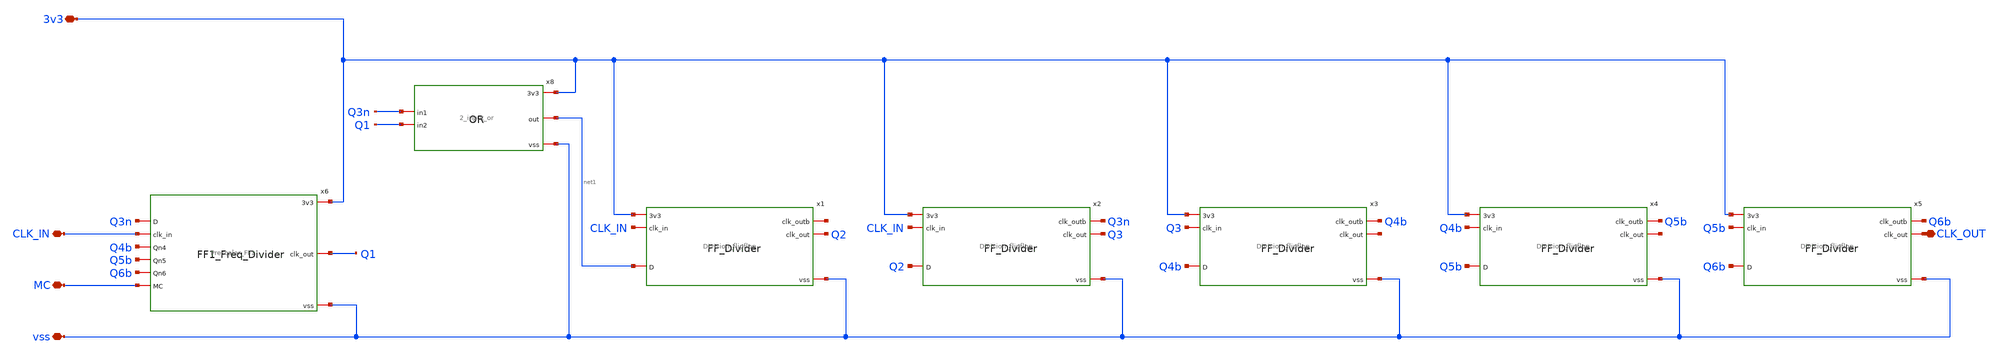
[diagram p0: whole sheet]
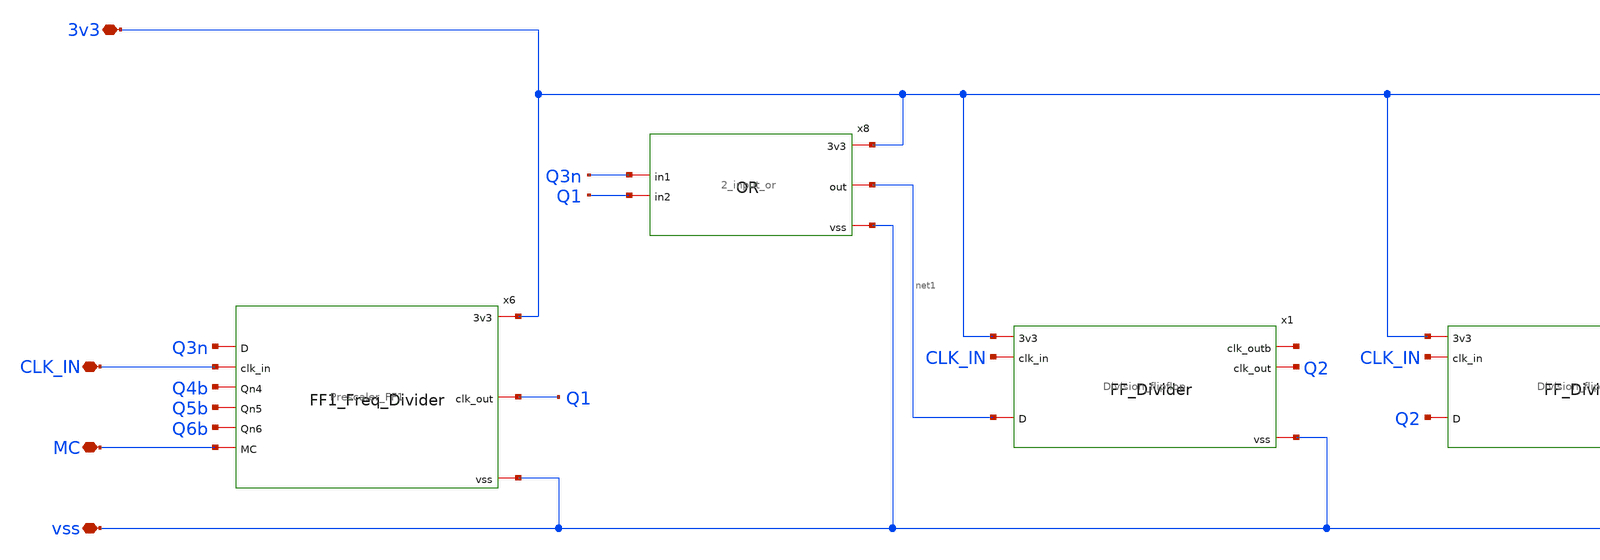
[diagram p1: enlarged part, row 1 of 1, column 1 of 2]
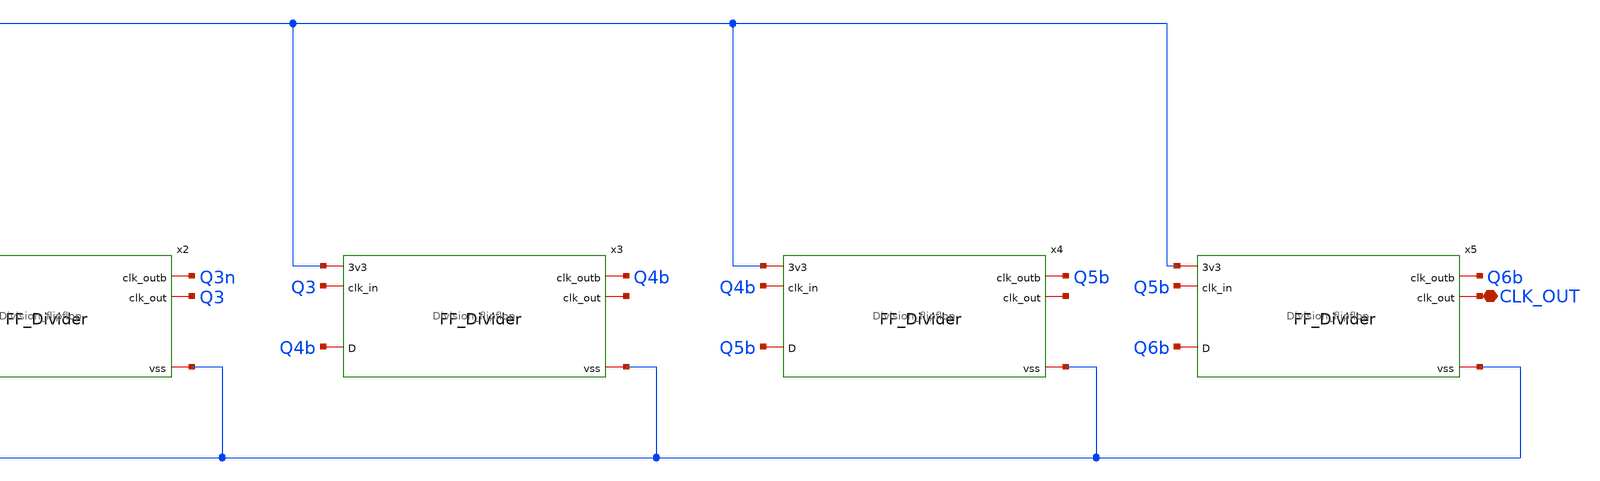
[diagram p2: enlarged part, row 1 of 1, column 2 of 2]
** sch_path: PLL/analog/schematics/32_33_Prescaler_Block.sch
**.subckt 32_33_Prescaler_Block CLK_IN MC 3v3 vss CLK_OUT
*.iopin CLK_IN
*.iopin MC
*.iopin 3v3
*.iopin vss
*.iopin CLK_OUT
x8 3v3 Q3n Q1 net1 vss 2_input_or
x6 3v3 Q1 Q3n CLK_IN Q4b Q5b Q6b MC vss Prescaler_FF1
x1 3v3 CLK_IN net2 Q2 net1 vss Division_flipflop
x2 3v3 CLK_IN Q3n Q3 Q2 vss Division_flipflop
x3 3v3 Q3 Q4b net3 Q4b vss Division_flipflop
x4 3v3 Q4b Q5b net4 Q5b vss Division_flipflop
x5 3v3 Q5b Q6b CLK_OUT Q6b vss Division_flipflop
**.ends

* expanding   symbol:  2_input_or.sym # of pins=5
** sym_path: PLL/analog/schematics/2_input_or.sym
** sch_path: PLL/analog/schematics/2_input_or.sch
.subckt 2_input_or 3v3 in1 in2 out vss
*.iopin in1
*.iopin in2
*.iopin out
*.iopin 3v3
*.iopin vss
XM1 net1 in1 3v3 3v3 pfet_03v3 L=0.36u W=0.72u nf=1 ad='int((nf+1)/2) * W/nf * 0.18u' as='int((nf+2)/2) * W/nf * 0.18u'
+ pd='2*int((nf+1)/2) * (W/nf + 0.18u)' ps='2*int((nf+2)/2) * (W/nf + 0.18u)' nrd='0.18u / W' nrs='0.18u / W'
+ sa=0 sb=0 sd=0 m=1
XM2 net2 in2 net1 3v3 pfet_03v3 L=0.36u W=0.72u nf=1 ad='int((nf+1)/2) * W/nf * 0.18u' as='int((nf+2)/2) * W/nf * 0.18u'
+ pd='2*int((nf+1)/2) * (W/nf + 0.18u)' ps='2*int((nf+2)/2) * (W/nf + 0.18u)' nrd='0.18u / W' nrs='0.18u / W'
+ sa=0 sb=0 sd=0 m=1
XM3 net2 in1 vss vss nfet_03v3 L=0.36u W=0.36u nf=1 ad='int((nf+1)/2) * W/nf * 0.18u' as='int((nf+2)/2) * W/nf * 0.18u'
+ pd='2*int((nf+1)/2) * (W/nf + 0.18u)' ps='2*int((nf+2)/2) * (W/nf + 0.18u)' nrd='0.18u / W' nrs='0.18u / W'
+ sa=0 sb=0 sd=0 m=1
XM4 net2 in2 vss vss nfet_03v3 L=0.36u W=0.36u nf=1 ad='int((nf+1)/2) * W/nf * 0.18u' as='int((nf+2)/2) * W/nf * 0.18u'
+ pd='2*int((nf+1)/2) * (W/nf + 0.18u)' ps='2*int((nf+2)/2) * (W/nf + 0.18u)' nrd='0.18u / W' nrs='0.18u / W'
+ sa=0 sb=0 sd=0 m=1
XM5 out net2 vss vss nfet_03v3 L=0.36u W=0.36u nf=1 ad='int((nf+1)/2) * W/nf * 0.18u' as='int((nf+2)/2) * W/nf * 0.18u'
+ pd='2*int((nf+1)/2) * (W/nf + 0.18u)' ps='2*int((nf+2)/2) * (W/nf + 0.18u)' nrd='0.18u / W' nrs='0.18u / W'
+ sa=0 sb=0 sd=0 m=1
XM6 out net2 3v3 3v3 pfet_03v3 L=0.36u W=0.72u nf=1 ad='int((nf+1)/2) * W/nf * 0.18u' as='int((nf+2)/2) * W/nf * 0.18u'
+ pd='2*int((nf+1)/2) * (W/nf + 0.18u)' ps='2*int((nf+2)/2) * (W/nf + 0.18u)' nrd='0.18u / W' nrs='0.18u / W'
+ sa=0 sb=0 sd=0 m=1
.ends


* expanding   symbol:  Prescaler_FF1.sym # of pins=9
** sym_path: PLL/analog/schematics/Prescaler_FF1.sym
** sch_path: PLL/analog/schematics/Prescaler_FF1.sch
.subckt Prescaler_FF1 3v3 clk_out D clk_in Qn4 Qn5 Qn6 MC vss
*.iopin D
*.iopin clk_in
*.iopin Qn4
*.iopin Qn5
*.iopin Qn6
*.iopin vss
*.iopin 3v3
*.iopin MC
*.iopin clk_out
XM1 net8 clk_in 3v3 3v3 pfet_03v3 L=0.32u W=0.72u nf=1 ad='int((nf+1)/2) * W/nf * 0.18u' as='int((nf+2)/2) * W/nf * 0.18u'
+ pd='2*int((nf+1)/2) * (W/nf + 0.18u)' ps='2*int((nf+2)/2) * (W/nf + 0.18u)' nrd='0.18u / W' nrs='0.18u / W'
+ sa=0 sb=0 sd=0 m=1
XM2 net1 D net8 3v3 pfet_03v3 L=0.32u W=0.72u nf=1 ad='int((nf+1)/2) * W/nf * 0.18u' as='int((nf+2)/2) * W/nf * 0.18u'
+ pd='2*int((nf+1)/2) * (W/nf + 0.18u)' ps='2*int((nf+2)/2) * (W/nf + 0.18u)' nrd='0.18u / W' nrs='0.18u / W'
+ sa=0 sb=0 sd=0 m=1
XM3 net1 D net2 vss nfet_03v3 L=0.32u W=0.36u nf=1 ad='int((nf+1)/2) * W/nf * 0.18u' as='int((nf+2)/2) * W/nf * 0.18u'
+ pd='2*int((nf+1)/2) * (W/nf + 0.18u)' ps='2*int((nf+2)/2) * (W/nf + 0.18u)' nrd='0.18u / W' nrs='0.18u / W'
+ sa=0 sb=0 sd=0 m=1
XM4 net2 clk_in net3 vss nfet_03v3 L=0.32u W=0.36u nf=1 ad='int((nf+1)/2) * W/nf * 0.18u' as='int((nf+2)/2) * W/nf * 0.18u'
+ pd='2*int((nf+1)/2) * (W/nf + 0.18u)' ps='2*int((nf+2)/2) * (W/nf + 0.18u)' nrd='0.18u / W' nrs='0.18u / W'
+ sa=0 sb=0 sd=0 m=1
XM5 net3 Qn4 net4 vss nfet_03v3 L=0.32u W=0.36u nf=1 ad='int((nf+1)/2) * W/nf * 0.18u' as='int((nf+2)/2) * W/nf * 0.18u'
+ pd='2*int((nf+1)/2) * (W/nf + 0.18u)' ps='2*int((nf+2)/2) * (W/nf + 0.18u)' nrd='0.18u / W' nrs='0.18u / W'
+ sa=0 sb=0 sd=0 m=1
XM6 net4 Qn5 net5 vss nfet_03v3 L=0.32u W=0.36u nf=1 ad='int((nf+1)/2) * W/nf * 0.18u' as='int((nf+2)/2) * W/nf * 0.18u'
+ pd='2*int((nf+1)/2) * (W/nf + 0.18u)' ps='2*int((nf+2)/2) * (W/nf + 0.18u)' nrd='0.18u / W' nrs='0.18u / W'
+ sa=0 sb=0 sd=0 m=1
XM7 net5 Qn6 net6 vss nfet_03v3 L=0.32u W=0.36u nf=1 ad='int((nf+1)/2) * W/nf * 0.18u' as='int((nf+2)/2) * W/nf * 0.18u'
+ pd='2*int((nf+1)/2) * (W/nf + 0.18u)' ps='2*int((nf+2)/2) * (W/nf + 0.18u)' nrd='0.18u / W' nrs='0.18u / W'
+ sa=0 sb=0 sd=0 m=1
XM8 net6 MC vss vss nfet_03v3 L=0.32u W=0.36u nf=1 ad='int((nf+1)/2) * W/nf * 0.18u' as='int((nf+2)/2) * W/nf * 0.18u'
+ pd='2*int((nf+1)/2) * (W/nf + 0.18u)' ps='2*int((nf+2)/2) * (W/nf + 0.18u)' nrd='0.18u / W' nrs='0.18u / W'
+ sa=0 sb=0 sd=0 m=1
XM9 clk_out net1 3v3 3v3 pfet_03v3 L=0.36u W=0.72u nf=1 ad='int((nf+1)/2) * W/nf * 0.18u' as='int((nf+2)/2) * W/nf * 0.18u'
+ pd='2*int((nf+1)/2) * (W/nf + 0.18u)' ps='2*int((nf+2)/2) * (W/nf + 0.18u)' nrd='0.18u / W' nrs='0.18u / W'
+ sa=0 sb=0 sd=0 m=1
XM10 clk_out net1 net7 vss nfet_03v3 L=0.36u W=0.36u nf=1 ad='int((nf+1)/2) * W/nf * 0.18u' as='int((nf+2)/2) * W/nf * 0.18u'
+ pd='2*int((nf+1)/2) * (W/nf + 0.18u)' ps='2*int((nf+2)/2) * (W/nf + 0.18u)' nrd='0.18u / W' nrs='0.18u / W'
+ sa=0 sb=0 sd=0 m=1
XM11 net7 clk_in vss vss nfet_03v3 L=0.36u W=0.36u nf=1 ad='int((nf+1)/2) * W/nf * 0.18u' as='int((nf+2)/2) * W/nf * 0.18u'
+ pd='2*int((nf+1)/2) * (W/nf + 0.18u)' ps='2*int((nf+2)/2) * (W/nf + 0.18u)' nrd='0.18u / W' nrs='0.18u / W'
+ sa=0 sb=0 sd=0 m=1
.ends


* expanding   symbol:  Division_flipflop.sym # of pins=6
** sym_path: PLL/analog/schematics/Division_flipflop.sym
** sch_path: PLL/analog/schematics/Division_flipflop.sch
.subckt Division_flipflop 3v3 clk_in clk_outb clk_out D vss
*.iopin 3v3
*.iopin vss
*.iopin clk_outb
*.iopin D
*.iopin clk_in
*.iopin clk_out
XM1 net3 clk_in vss vss nfet_03v3 L=0.36u W=0.56u nf=1 ad='int((nf+1)/2) * W/nf * 0.18u' as='int((nf+2)/2) * W/nf * 0.18u'
+ pd='2*int((nf+1)/2) * (W/nf + 0.18u)' ps='2*int((nf+2)/2) * (W/nf + 0.18u)' nrd='0.18u / W' nrs='0.18u / W'
+ sa=0 sb=0 sd=0 m=1
XM2 net2 D vss vss nfet_03v3 L=0.36u W=0.56u nf=1 ad='int((nf+1)/2) * W/nf * 0.18u' as='int((nf+2)/2) * W/nf * 0.18u'
+ pd='2*int((nf+1)/2) * (W/nf + 0.18u)' ps='2*int((nf+2)/2) * (W/nf + 0.18u)' nrd='0.18u / W' nrs='0.18u / W'
+ sa=0 sb=0 sd=0 m=1
XM3 net5 net4 vss vss nfet_03v3 L=0.36u W=0.56u nf=1 ad='int((nf+1)/2) * W/nf * 0.18u' as='int((nf+2)/2) * W/nf * 0.18u'
+ pd='2*int((nf+1)/2) * (W/nf + 0.18u)' ps='2*int((nf+2)/2) * (W/nf + 0.18u)' nrd='0.18u / W' nrs='0.18u / W'
+ sa=0 sb=0 sd=0 m=1
XM4 clk_outb clk_in net5 vss nfet_03v3 L=0.36u W=0.56u nf=1 ad='int((nf+1)/2) * W/nf * 0.18u' as='int((nf+2)/2) * W/nf * 0.18u'
+ pd='2*int((nf+1)/2) * (W/nf + 0.18u)' ps='2*int((nf+2)/2) * (W/nf + 0.18u)' nrd='0.18u / W' nrs='0.18u / W'
+ sa=0 sb=0 sd=0 m=1
XM5 net1 D 3v3 3v3 pfet_03v3 L=0.36u W=1.12u nf=1 ad='int((nf+1)/2) * W/nf * 0.18u' as='int((nf+2)/2) * W/nf * 0.18u'
+ pd='2*int((nf+1)/2) * (W/nf + 0.18u)' ps='2*int((nf+2)/2) * (W/nf + 0.18u)' nrd='0.18u / W' nrs='0.18u / W'
+ sa=0 sb=0 sd=0 m=1
XM6 net2 clk_in net1 3v3 pfet_03v3 L=0.36u W=1.12u nf=1 ad='int((nf+1)/2) * W/nf * 0.18u' as='int((nf+2)/2) * W/nf * 0.18u'
+ pd='2*int((nf+1)/2) * (W/nf + 0.18u)' ps='2*int((nf+2)/2) * (W/nf + 0.18u)' nrd='0.18u / W' nrs='0.18u / W'
+ sa=0 sb=0 sd=0 m=1
XM8 net4 clk_in 3v3 3v3 pfet_03v3 L=0.36u W=1.12u nf=1 ad='int((nf+1)/2) * W/nf * 0.18u' as='int((nf+2)/2) * W/nf * 0.18u'
+ pd='2*int((nf+1)/2) * (W/nf + 0.18u)' ps='2*int((nf+2)/2) * (W/nf + 0.18u)' nrd='0.18u / W' nrs='0.18u / W'
+ sa=0 sb=0 sd=0 m=1
XM9 clk_outb net4 3v3 3v3 pfet_03v3 L=0.36u W=1.12u nf=1 ad='int((nf+1)/2) * W/nf * 0.18u' as='int((nf+2)/2) * W/nf * 0.18u'
+ pd='2*int((nf+1)/2) * (W/nf + 0.18u)' ps='2*int((nf+2)/2) * (W/nf + 0.18u)' nrd='0.18u / W' nrs='0.18u / W'
+ sa=0 sb=0 sd=0 m=1
XM7 net4 net2 net3 vss nfet_03v3 L=0.36u W=0.56u nf=1 ad='int((nf+1)/2) * W/nf * 0.18u' as='int((nf+2)/2) * W/nf * 0.18u'
+ pd='2*int((nf+1)/2) * (W/nf + 0.18u)' ps='2*int((nf+2)/2) * (W/nf + 0.18u)' nrd='0.18u / W' nrs='0.18u / W'
+ sa=0 sb=0 sd=0 m=1
XM10 clk_out clk_outb 3v3 3v3 pfet_03v3 L=0.36u W=1.12u nf=1 ad='int((nf+1)/2) * W/nf * 0.18u' as='int((nf+2)/2) * W/nf * 0.18u'
+ pd='2*int((nf+1)/2) * (W/nf + 0.18u)' ps='2*int((nf+2)/2) * (W/nf + 0.18u)' nrd='0.18u / W' nrs='0.18u / W'
+ sa=0 sb=0 sd=0 m=1
XM11 clk_out clk_outb vss vss nfet_03v3 L=0.36u W=0.56u nf=1 ad='int((nf+1)/2) * W/nf * 0.18u' as='int((nf+2)/2) * W/nf * 0.18u'
+ pd='2*int((nf+1)/2) * (W/nf + 0.18u)' ps='2*int((nf+2)/2) * (W/nf + 0.18u)' nrd='0.18u / W' nrs='0.18u / W'
+ sa=0 sb=0 sd=0 m=1
.ends

.end
